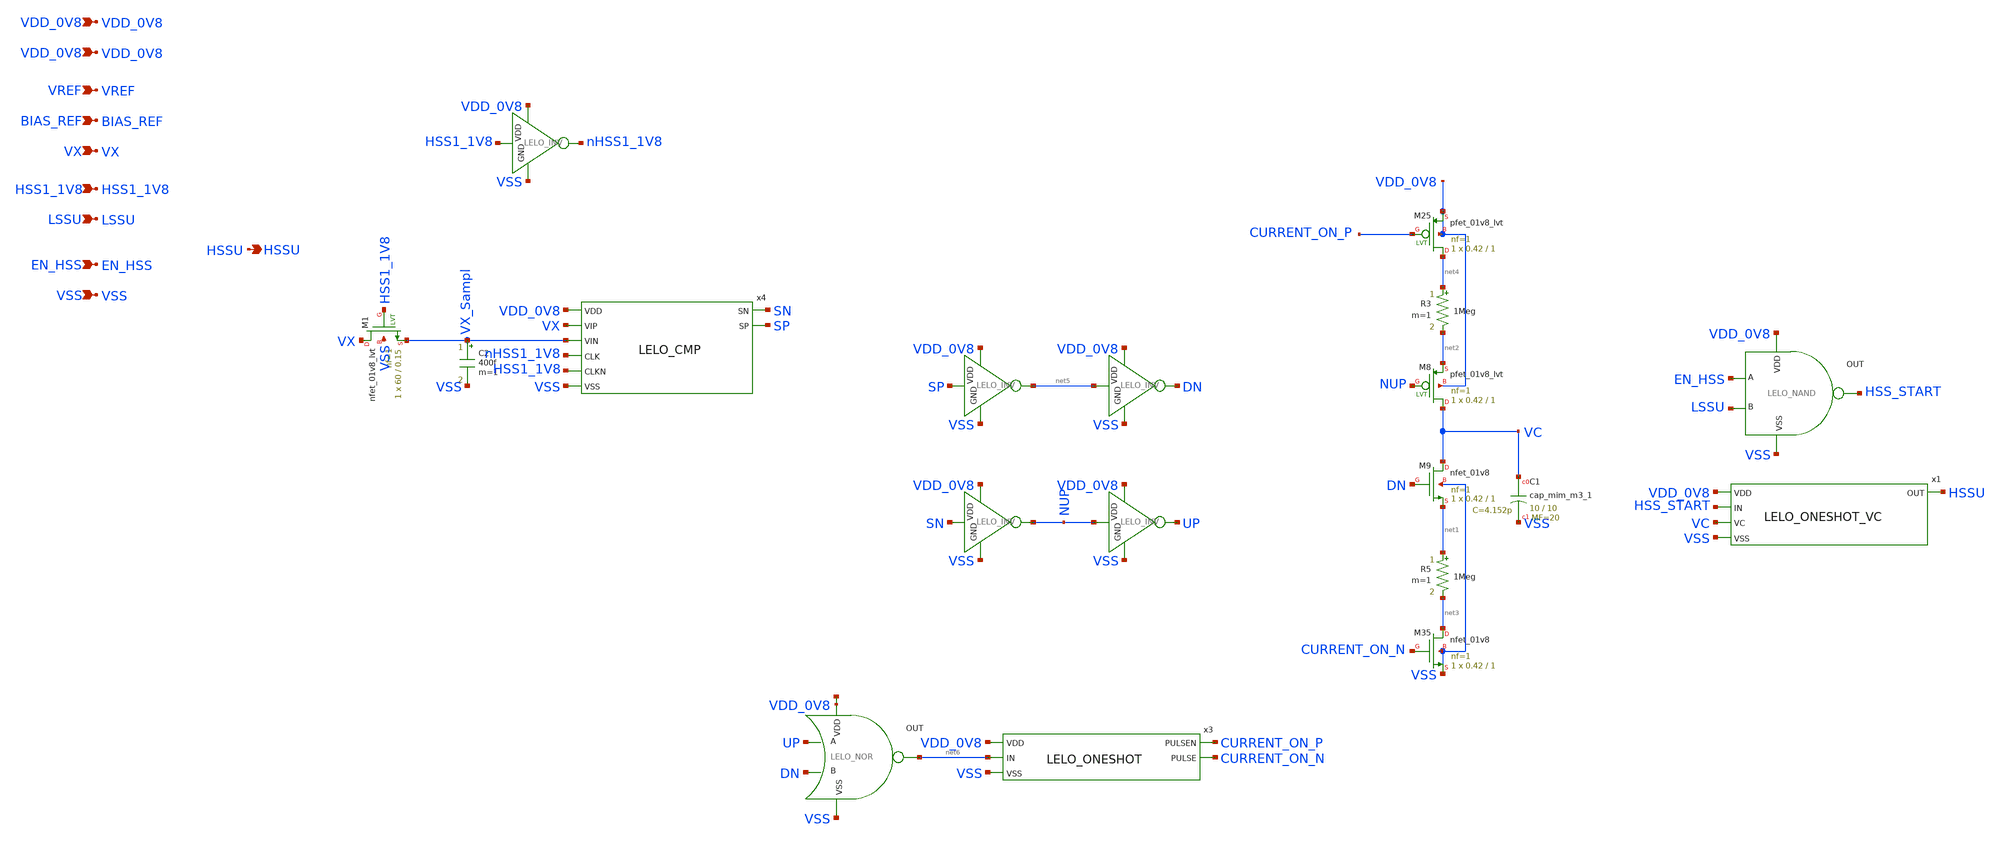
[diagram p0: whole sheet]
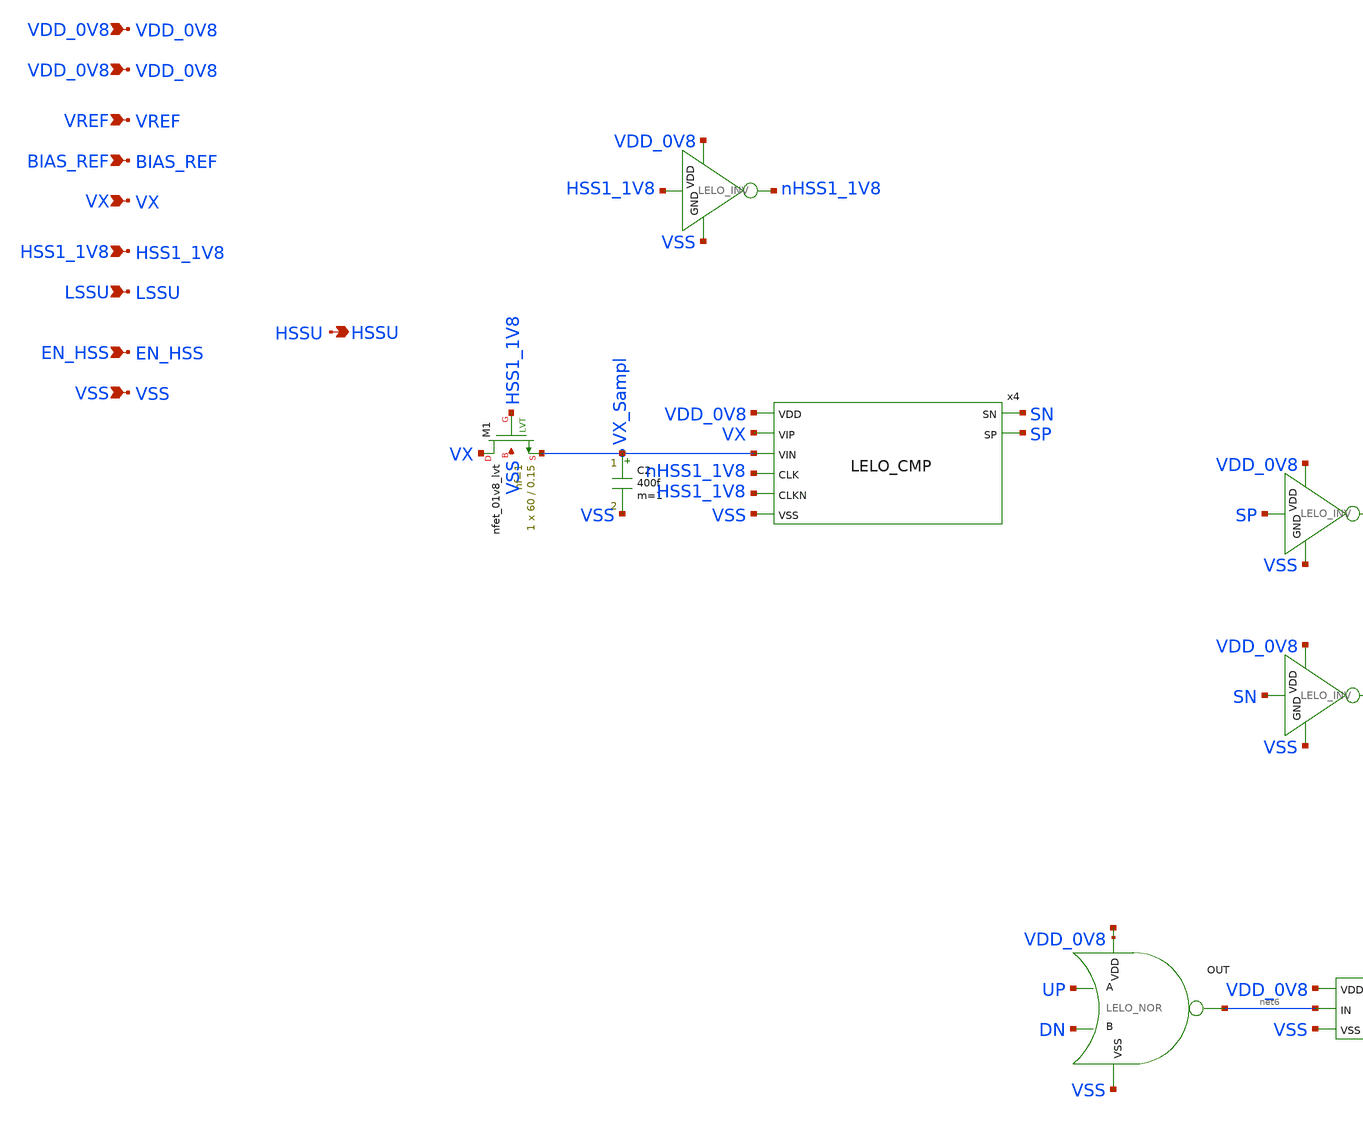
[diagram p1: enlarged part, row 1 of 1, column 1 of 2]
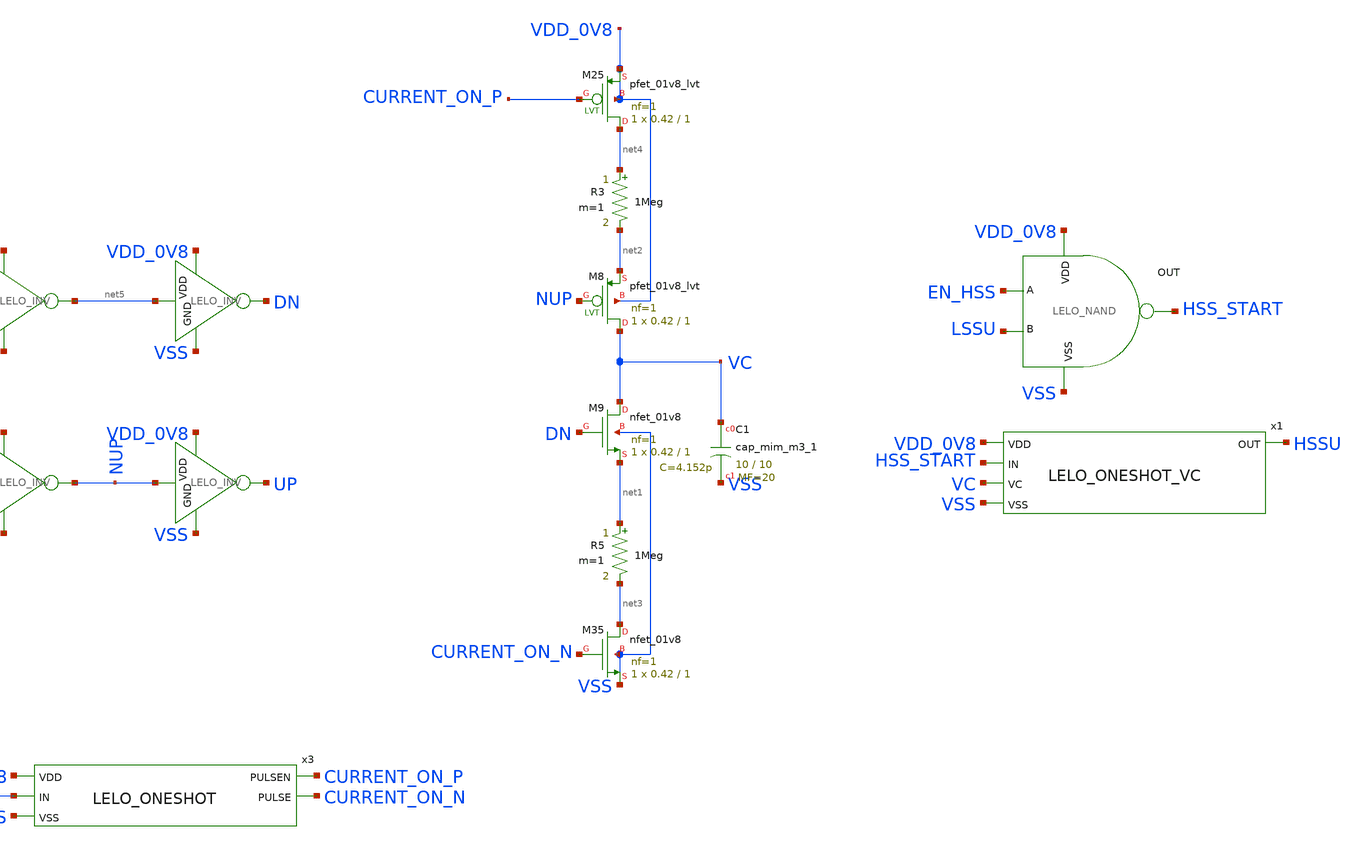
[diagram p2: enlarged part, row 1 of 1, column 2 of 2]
** sch_path: design/LELO_SVOD_SKY130A/LELO_SVOD_HSSCNTRL.sch
**.subckt LELO_SVOD_HSSCNTRL VREF HSSU VX LSSU VSS EN_HSS VDD_0V8 HSS1_1V8 BIAS_REF VDD_0V8
*.ipin VREF
*.opin HSSU
*.ipin VX
*.ipin LSSU
*.ipin VSS
*.ipin EN_HSS
*.ipin VDD_0V8
*.ipin HSS1_1V8
*.ipin BIAS_REF
*.ipin VDD_0V8
x4 SN SP VDD_0V8 VX VX_Sampl nHSS1_1V8 HSS1_1V8 VSS LELO_CMP
XM9 VC DN net1 VSS sky130_fd_pr__nfet_01v8 L=1 W=0.42 nf=1 ad='int((1 + 1)/2) * 0.42 / 1 * 0.29' as='int((1 + 2)/2) * 0.42 / 1 * 0.29'
+ pd='2*int((1 + 1)/2) * (0.42 / 1 + 0.29)' ps='2*int((1 + 2)/2) * (0.42 / 1 + 0.29)' nrd='0.29 / 0.42 '
+ nrs='0.29 / 0.42 ' sa=0 sb=0 sd=0 mult=1 m=1
x10 VDD_0V8 SP net5 VSS LELO_INV
R5 net1 net3 1Meg m=1
XM35 net3 CURRENT_ON_N VSS VSS sky130_fd_pr__nfet_01v8 L=1 W=0.42 nf=1 ad='int((1 + 1)/2) * 0.42 / 1 * 0.29'
+ as='int((1 + 2)/2) * 0.42 / 1 * 0.29' pd='2*int((1 + 1)/2) * (0.42 / 1 + 0.29)' ps='2*int((1 + 2)/2) * (0.42 / 1 + 0.29)'
+ nrd='0.29 / 0.42 ' nrs='0.29 / 0.42 ' sa=0 sb=0 sd=0 mult=1 m=1
x11 VDD_0V8 SN NUP VSS LELO_INV
x14 VDD_0V8 NUP UP VSS LELO_INV
x17 VDD_0V8 net5 DN VSS LELO_INV
x2 net7 net6 UP DN VSS LELO_NOR
x3 VDD_0V8 net6 VSS CURRENT_ON_P CURRENT_ON_N LELO_ONESHOT
R3 net4 net2 1Meg m=1
XM8 VC NUP net2 VDD_0V8 sky130_fd_pr__pfet_01v8_lvt L=1 W=0.42 nf=1 ad='int((1 + 1)/2) * 0.42 / 1 * 0.29'
+ as='int((1 + 2)/2) * 0.42 / 1 * 0.29' pd='2*int((1 + 1)/2) * (0.42 / 1 + 0.29)' ps='2*int((1 + 2)/2) * (0.42 / 1 + 0.29)'
+ nrd='0.29 / 0.42 ' nrs='0.29 / 0.42 ' sa=0 sb=0 sd=0 mult=1 m=1
XM25 net4 CURRENT_ON_P VDD_0V8 VDD_0V8 sky130_fd_pr__pfet_01v8_lvt L=1 W=0.42 nf=1 ad='int((1 + 1)/2) * 0.42 / 1 * 0.29'
+ as='int((1 + 2)/2) * 0.42 / 1 * 0.29' pd='2*int((1 + 1)/2) * (0.42 / 1 + 0.29)' ps='2*int((1 + 2)/2) * (0.42 / 1 + 0.29)'
+ nrd='0.29 / 0.42 ' nrs='0.29 / 0.42 ' sa=0 sb=0 sd=0 mult=1 m=1
x1 VDD_0V8 HSS_START VC HSSU VSS LELO_ONESHOT_VC
x6 VDD_0V8 HSS_START EN_HSS LSSU VSS LELO_NAND
XC1 VC VSS sky130_fd_pr__cap_mim_m3_1 W=10 L=10 MF=20 m=20
C2 VX_Sampl VSS 400f m=1
XM1 VX HSS1_1V8 VX_Sampl VSS sky130_fd_pr__nfet_01v8_lvt L=0.15 W=60 nf=1 ad='int((1 + 1)/2) * 60 / 1 * 0.29'
+ as='int((1 + 2)/2) * 60 / 1 * 0.29' pd='2*int((1 + 1)/2) * (60 / 1 + 0.29)' ps='2*int((1 + 2)/2) * (60 / 1 + 0.29)'
+ nrd='0.29 / 60 ' nrs='0.29 / 60 ' sa=0 sb=0 sd=0 mult=1 m=1
x5 VDD_0V8 HSS1_1V8 nHSS1_1V8 VSS LELO_INV
**.ends

* expanding   symbol:  LELO_SVOD_SKY130A/LELO_CMP.sym # of pins=8
** sym_path: design/LELO_SVOD_SKY130A/LELO_CMP.sym
** sch_path: design/LELO_SVOD_SKY130A/LELO_CMP.sch
.subckt LELO_CMP SN SP VDD VIP VIN CLK CLKN VSS
*.ipin VIP
*.ipin VIN
*.ipin CLK
*.ipin CLKN
*.ipin VDD
*.ipin VSS
*.opin SN
*.opin SP
XM2 SN net3 net5 VDD sky130_fd_pr__pfet_01v8_lvt L=0.44 W=1.92 nf=2 ad='int((2 + 1)/2) * 1.92 / 2 * 0.29'
+ as='int((2 + 2)/2) * 1.92 / 2 * 0.29' pd='2*int((2 + 1)/2) * (1.92 / 2 + 0.29)' ps='2*int((2 + 2)/2) * (1.92 / 2 + 0.29)'
+ nrd='0.29 / 1.92 ' nrs='0.29 / 1.92 ' sa=0 sb=0 sd=0 mult=3 m=3
XM1 SP net2 net6 VDD sky130_fd_pr__pfet_01v8_lvt L=0.44 W=1.92 nf=2 ad='int((2 + 1)/2) * 1.92 / 2 * 0.29'
+ as='int((2 + 2)/2) * 1.92 / 2 * 0.29' pd='2*int((2 + 1)/2) * (1.92 / 2 + 0.29)' ps='2*int((2 + 2)/2) * (1.92 / 2 + 0.29)'
+ nrd='0.29 / 1.92 ' nrs='0.29 / 1.92 ' sa=0 sb=0 sd=0 mult=3 m=3
XM3 net2 VIP net1 VSS sky130_fd_pr__nfet_01v8_lvt L=0.44 W=6.4 nf=1 ad='int((1 + 1)/2) * 6.4 / 1 * 0.29'
+ as='int((1 + 2)/2) * 6.4 / 1 * 0.29' pd='2*int((1 + 1)/2) * (6.4 / 1 + 0.29)' ps='2*int((1 + 2)/2) * (6.4 / 1 + 0.29)'
+ nrd='0.29 / 6.4 ' nrs='0.29 / 6.4 ' sa=0 sb=0 sd=0 mult=1 m=1
XM4 net3 VIN net1 VSS sky130_fd_pr__nfet_01v8_lvt L=0.44 W=6.4 nf=1 ad='int((1 + 1)/2) * 6.4 / 1 * 0.29'
+ as='int((1 + 2)/2) * 6.4 / 1 * 0.29' pd='2*int((1 + 1)/2) * (6.4 / 1 + 0.29)' ps='2*int((1 + 2)/2) * (6.4 / 1 + 0.29)'
+ nrd='0.29 / 6.4 ' nrs='0.29 / 6.4 ' sa=0 sb=0 sd=0 mult=1 m=1
XM5 net3 CLK VDD VDD sky130_fd_pr__pfet_01v8_lvt L=0.94 W=1.92 nf=2 ad='int((2 + 1)/2) * 1.92 / 2 * 0.29'
+ as='int((2 + 2)/2) * 1.92 / 2 * 0.29' pd='2*int((2 + 1)/2) * (1.92 / 2 + 0.29)' ps='2*int((2 + 2)/2) * (1.92 / 2 + 0.29)'
+ nrd='0.29 / 1.92 ' nrs='0.29 / 1.92 ' sa=0 sb=0 sd=0 mult=1 m=1
XM6 net6 SN VDD VDD sky130_fd_pr__pfet_01v8_lvt L=0.94 W=1.92 nf=2 ad='int((2 + 1)/2) * 1.92 / 2 * 0.29'
+ as='int((2 + 2)/2) * 1.92 / 2 * 0.29' pd='2*int((2 + 1)/2) * (1.92 / 2 + 0.29)' ps='2*int((2 + 2)/2) * (1.92 / 2 + 0.29)'
+ nrd='0.29 / 1.92 ' nrs='0.29 / 1.92 ' sa=0 sb=0 sd=0 mult=1 m=1
XM7 net5 SP VDD VDD sky130_fd_pr__pfet_01v8_lvt L=0.94 W=1.92 nf=2 ad='int((2 + 1)/2) * 1.92 / 2 * 0.29'
+ as='int((2 + 2)/2) * 1.92 / 2 * 0.29' pd='2*int((2 + 1)/2) * (1.92 / 2 + 0.29)' ps='2*int((2 + 2)/2) * (1.92 / 2 + 0.29)'
+ nrd='0.29 / 1.92 ' nrs='0.29 / 1.92 ' sa=0 sb=0 sd=0 mult=1 m=1
XM8 net2 CLK VDD VDD sky130_fd_pr__pfet_01v8_lvt L=0.94 W=1.92 nf=2 ad='int((2 + 1)/2) * 1.92 / 2 * 0.29'
+ as='int((2 + 2)/2) * 1.92 / 2 * 0.29' pd='2*int((2 + 1)/2) * (1.92 / 2 + 0.29)' ps='2*int((2 + 2)/2) * (1.92 / 2 + 0.29)'
+ nrd='0.29 / 1.92 ' nrs='0.29 / 1.92 ' sa=0 sb=0 sd=0 mult=1 m=1
XM9 net1 CLK net4 VSS sky130_fd_pr__nfet_01v8 L=0.94 W=1.92 nf=2 ad='int((2 + 1)/2) * 1.92 / 2 * 0.29'
+ as='int((2 + 2)/2) * 1.92 / 2 * 0.29' pd='2*int((2 + 1)/2) * (1.92 / 2 + 0.29)' ps='2*int((2 + 2)/2) * (1.92 / 2 + 0.29)'
+ nrd='0.29 / 1.92 ' nrs='0.29 / 1.92 ' sa=0 sb=0 sd=0 mult=1 m=1
XM10 net4 CLK VSS VSS sky130_fd_pr__nfet_01v8 L=0.94 W=1.92 nf=2 ad='int((2 + 1)/2) * 1.92 / 2 * 0.29'
+ as='int((2 + 2)/2) * 1.92 / 2 * 0.29' pd='2*int((2 + 1)/2) * (1.92 / 2 + 0.29)' ps='2*int((2 + 2)/2) * (1.92 / 2 + 0.29)'
+ nrd='0.29 / 1.92 ' nrs='0.29 / 1.92 ' sa=0 sb=0 sd=0 mult=1 m=1
XM11 SN CLKN VSS VSS sky130_fd_pr__nfet_01v8 L=0.94 W=1.92 nf=2 ad='int((2 + 1)/2) * 1.92 / 2 * 0.29'
+ as='int((2 + 2)/2) * 1.92 / 2 * 0.29' pd='2*int((2 + 1)/2) * (1.92 / 2 + 0.29)' ps='2*int((2 + 2)/2) * (1.92 / 2 + 0.29)'
+ nrd='0.29 / 1.92 ' nrs='0.29 / 1.92 ' sa=0 sb=0 sd=0 mult=1 m=1
XM12 SP SN VSS VSS sky130_fd_pr__nfet_01v8 L=0.94 W=1.92 nf=2 ad='int((2 + 1)/2) * 1.92 / 2 * 0.29' as='int((2 + 2)/2) * 1.92 / 2 * 0.29'
+ pd='2*int((2 + 1)/2) * (1.92 / 2 + 0.29)' ps='2*int((2 + 2)/2) * (1.92 / 2 + 0.29)' nrd='0.29 / 1.92 '
+ nrs='0.29 / 1.92 ' sa=0 sb=0 sd=0 mult=1 m=1
XM13 SN SP VSS VSS sky130_fd_pr__nfet_01v8 L=0.94 W=1.92 nf=2 ad='int((2 + 1)/2) * 1.92 / 2 * 0.29' as='int((2 + 2)/2) * 1.92 / 2 * 0.29'
+ pd='2*int((2 + 1)/2) * (1.92 / 2 + 0.29)' ps='2*int((2 + 2)/2) * (1.92 / 2 + 0.29)' nrd='0.29 / 1.92 '
+ nrs='0.29 / 1.92 ' sa=0 sb=0 sd=0 mult=1 m=1
XM14 SP CLKN VSS VSS sky130_fd_pr__nfet_01v8 L=0.94 W=1.92 nf=2 ad='int((2 + 1)/2) * 1.92 / 2 * 0.29'
+ as='int((2 + 2)/2) * 1.92 / 2 * 0.29' pd='2*int((2 + 1)/2) * (1.92 / 2 + 0.29)' ps='2*int((2 + 2)/2) * (1.92 / 2 + 0.29)'
+ nrd='0.29 / 1.92 ' nrs='0.29 / 1.92 ' sa=0 sb=0 sd=0 mult=1 m=1
.ends


* expanding   symbol:  LELO_SVOD_SKY130A/LELO_INV.sym # of pins=4
** sym_path: design/LELO_SVOD_SKY130A/LELO_INV.sym
** sch_path: design/LELO_SVOD_SKY130A/LELO_INV.sch
.subckt LELO_INV VDD VIN VOUT GND
*.ipin VIN
*.ipin VDD
*.ipin GND
*.opin VOUT
XM1 VOUT VIN GND GND sky130_fd_pr__nfet_01v8_lvt L=0.15 W=1 nf=1 ad='int((1 + 1)/2) * 1 / 1 * 0.29' as='int((1 + 2)/2) * 1 / 1 * 0.29'
+ pd='2*int((1 + 1)/2) * (1 / 1 + 0.29)' ps='2*int((1 + 2)/2) * (1 / 1 + 0.29)' nrd='0.29 / 1 ' nrs='0.29 / 1 '
+ sa=0 sb=0 sd=0 mult=1 m=1
XM2 VOUT VIN VDD VDD sky130_fd_pr__pfet_01v8_lvt L=0.35 W=1 nf=1 ad='int((1 + 1)/2) * 1 / 1 * 0.29' as='int((1 + 2)/2) * 1 / 1 * 0.29'
+ pd='2*int((1 + 1)/2) * (1 / 1 + 0.29)' ps='2*int((1 + 2)/2) * (1 / 1 + 0.29)' nrd='0.29 / 1 ' nrs='0.29 / 1 '
+ sa=0 sb=0 sd=0 mult=2 m=2
.ends


* expanding   symbol:  LELO_SVOD_SKY130A/LELO_NOR.sym # of pins=5
** sym_path: design/LELO_SVOD_SKY130A/LELO_NOR.sym
** sch_path: design/LELO_SVOD_SKY130A/LELO_NOR.sch
.subckt LELO_NOR VDD OUT A B VSS
*.ipin VDD
*.ipin VSS
*.opin OUT
*.ipin A
*.ipin B
XM2 OUT B VSS VSS sky130_fd_pr__nfet_01v8 L=0.15 W=2 nf=1 ad='int((1 + 1)/2) * 2 / 1 * 0.29' as='int((1 + 2)/2) * 2 / 1 * 0.29'
+ pd='2*int((1 + 1)/2) * (2 / 1 + 0.29)' ps='2*int((1 + 2)/2) * (2 / 1 + 0.29)' nrd='0.29 / 2 ' nrs='0.29 / 2 '
+ sa=0 sb=0 sd=0 mult=1 m=1
XM1 OUT A VSS VSS sky130_fd_pr__nfet_01v8 L=0.15 W=2 nf=1 ad='int((1 + 1)/2) * 2 / 1 * 0.29' as='int((1 + 2)/2) * 2 / 1 * 0.29'
+ pd='2*int((1 + 1)/2) * (2 / 1 + 0.29)' ps='2*int((1 + 2)/2) * (2 / 1 + 0.29)' nrd='0.29 / 2 ' nrs='0.29 / 2 '
+ sa=0 sb=0 sd=0 mult=1 m=1
XM3 OUT B net1 VDD sky130_fd_pr__pfet_01v8 L=0.15 W=4 nf=1 ad='int((1 + 1)/2) * 4 / 1 * 0.29' as='int((1 + 2)/2) * 4 / 1 * 0.29'
+ pd='2*int((1 + 1)/2) * (4 / 1 + 0.29)' ps='2*int((1 + 2)/2) * (4 / 1 + 0.29)' nrd='0.29 / 4 ' nrs='0.29 / 4 '
+ sa=0 sb=0 sd=0 mult=1 m=1
XM4 net1 A VDD VDD sky130_fd_pr__pfet_01v8 L=0.15 W=4 nf=1 ad='int((1 + 1)/2) * 4 / 1 * 0.29' as='int((1 + 2)/2) * 4 / 1 * 0.29'
+ pd='2*int((1 + 1)/2) * (4 / 1 + 0.29)' ps='2*int((1 + 2)/2) * (4 / 1 + 0.29)' nrd='0.29 / 4 ' nrs='0.29 / 4 '
+ sa=0 sb=0 sd=0 mult=1 m=1
.ends


* expanding   symbol:  LELO_SVOD_SKY130A/LELO_ONESHOT.sym # of pins=5
** sym_path: design/LELO_SVOD_SKY130A/LELO_ONESHOT.sym
** sch_path: design/LELO_SVOD_SKY130A/LELO_ONESHOT.sch
.subckt LELO_ONESHOT VDD IN VSS PULSEN PULSE
*.ipin VDD
*.ipin IN
*.ipin VSS
*.opin PULSEN
*.opin PULSE
x8 VDD PULSEN PULSE VSS LELO_INV
x12 net6 net3 net1 PULSE VSS LELO_NOR
C6 net2 net4 150f m=1
x13 VDD net2 PULSEN VSS LELO_INV
x18 VDD IN net1 VSS LELO_INV
x1 VDD net3 net4 VSS LELO_INV
XM1 net2 VDD net5 net5 sky130_fd_pr__nfet_01v8 L=0.15 W=1 nf=1 ad='int((1 + 1)/2) * 1 / 1 * 0.29' as='int((1 + 2)/2) * 1 / 1 * 0.29'
+ pd='2*int((1 + 1)/2) * (1 / 1 + 0.29)' ps='2*int((1 + 2)/2) * (1 / 1 + 0.29)' nrd='0.29 / 1 ' nrs='0.29 / 1 '
+ sa=0 sb=0 sd=0 mult=1 m=1
x2 VDD net3 net4 VSS LELO_INV
XR1 VSS net5 net5 sky130_fd_pr__res_xhigh_po_0p35 L=30 mult=1 m=1
.ends


* expanding   symbol:  LELO_SVOD_SKY130A/LELO_ONESHOT_VC.sym # of pins=5
** sym_path: design/LELO_SVOD_SKY130A/LELO_ONESHOT_VC.sym
** sch_path: design/LELO_SVOD_SKY130A/LELO_ONESHOT_VC.sch
.subckt LELO_ONESHOT_VC VDD IN VC OUT VSS
*.ipin VDD
*.ipin IN
*.ipin VC
*.ipin VSS
*.opin OUT
x2 net6 net2 OUT IN VSS LELO_NOR
C5 net1 net3 300f m=1
XM1 net1 VDD net5 net5 sky130_fd_pr__nfet_01v8 L=0.15 W=1 nf=1 ad='int((1 + 1)/2) * 1 / 1 * 0.29' as='int((1 + 2)/2) * 1 / 1 * 0.29'
+ pd='2*int((1 + 1)/2) * (1 / 1 + 0.29)' ps='2*int((1 + 2)/2) * (1 / 1 + 0.29)' nrd='0.29 / 1 ' nrs='0.29 / 1 '
+ sa=0 sb=0 sd=0 mult=1 m=1
XM2 net1 VC VSS VSS sky130_fd_pr__nfet_05v0_nvt L=20 W=0.5 nf=1 ad='int((1 + 1)/2) * 0.5 / 1 * 0.29'
+ as='int((1 + 2)/2) * 0.5 / 1 * 0.29' pd='2*int((1 + 1)/2) * (0.5 / 1 + 0.29)' ps='2*int((1 + 2)/2) * (0.5 / 1 + 0.29)'
+ nrd='0.29 / 0.5 ' nrs='0.29 / 0.5 ' sa=0 sb=0 sd=0 mult=1 m=1
XR1 VSS net5 net5 sky130_fd_pr__res_xhigh_po_0p35 L=150 mult=1 m=1
x1 VDD net1 net4 VSS LELO_INV_PVT
x3 VDD net4 OUT VSS LELO_INV_PVT
x4 VDD net2 net3 VSS LELO_INV
.ends


* expanding   symbol:  LELO_SVOD_SKY130A/LELO_NAND.sym # of pins=5
** sym_path: design/LELO_SVOD_SKY130A/LELO_NAND.sym
** sch_path: design/LELO_SVOD_SKY130A/LELO_NAND.sch
.subckt LELO_NAND VDD OUT A B VSS
*.ipin VDD
*.ipin VSS
*.opin OUT
*.ipin A
*.ipin B
XM1 net1 A VSS VSS sky130_fd_pr__nfet_01v8_lvt L=0.15 W=1 nf=1 ad='int((1 + 1)/2) * 1 / 1 * 0.29' as='int((1 + 2)/2) * 1 / 1 * 0.29'
+ pd='2*int((1 + 1)/2) * (1 / 1 + 0.29)' ps='2*int((1 + 2)/2) * (1 / 1 + 0.29)' nrd='0.29 / 1 ' nrs='0.29 / 1 '
+ sa=0 sb=0 sd=0 mult=1 m=1
XM2 OUT B net1 net1 sky130_fd_pr__nfet_01v8_lvt L=0.15 W=1 nf=1 ad='int((1 + 1)/2) * 1 / 1 * 0.29' as='int((1 + 2)/2) * 1 / 1 * 0.29'
+ pd='2*int((1 + 1)/2) * (1 / 1 + 0.29)' ps='2*int((1 + 2)/2) * (1 / 1 + 0.29)' nrd='0.29 / 1 ' nrs='0.29 / 1 '
+ sa=0 sb=0 sd=0 mult=1 m=1
XM3 OUT A VDD VDD sky130_fd_pr__pfet_01v8_lvt L=0.35 W=1 nf=1 ad='int((1 + 1)/2) * 1 / 1 * 0.29' as='int((1 + 2)/2) * 1 / 1 * 0.29'
+ pd='2*int((1 + 1)/2) * (1 / 1 + 0.29)' ps='2*int((1 + 2)/2) * (1 / 1 + 0.29)' nrd='0.29 / 1 ' nrs='0.29 / 1 '
+ sa=0 sb=0 sd=0 mult=1 m=1
XM4 OUT B VDD VDD sky130_fd_pr__pfet_01v8_lvt L=0.35 W=1 nf=1 ad='int((1 + 1)/2) * 1 / 1 * 0.29' as='int((1 + 2)/2) * 1 / 1 * 0.29'
+ pd='2*int((1 + 1)/2) * (1 / 1 + 0.29)' ps='2*int((1 + 2)/2) * (1 / 1 + 0.29)' nrd='0.29 / 1 ' nrs='0.29 / 1 '
+ sa=0 sb=0 sd=0 mult=1 m=1
.ends


* expanding   symbol:  LELO_SVOD_SKY130A/LELO_INV_PVT.sym # of pins=4
** sym_path: design/LELO_SVOD_SKY130A/LELO_INV_PVT.sym
** sch_path: design/LELO_SVOD_SKY130A/LELO_INV_PVT.sch
.subckt LELO_INV_PVT VDD VIN VOUT VSS
*.ipin VIN
*.ipin VDD
*.ipin VSS
*.opin VOUT
XM1 VOUT VIN VSS VSS sky130_fd_pr__nfet_01v8 L=0.5 W=4 nf=1 ad='int((1 + 1)/2) * 4 / 1 * 0.29' as='int((1 + 2)/2) * 4 / 1 * 0.29'
+ pd='2*int((1 + 1)/2) * (4 / 1 + 0.29)' ps='2*int((1 + 2)/2) * (4 / 1 + 0.29)' nrd='0.29 / 4 ' nrs='0.29 / 4 '
+ sa=0 sb=0 sd=0 mult=1 m=1
XM2 VOUT VIN VDD VDD sky130_fd_pr__pfet_01v8_lvt L=1 W=4 nf=1 ad='int((1 + 1)/2) * 4 / 1 * 0.29' as='int((1 + 2)/2) * 4 / 1 * 0.29'
+ pd='2*int((1 + 1)/2) * (4 / 1 + 0.29)' ps='2*int((1 + 2)/2) * (4 / 1 + 0.29)' nrd='0.29 / 4 ' nrs='0.29 / 4 '
+ sa=0 sb=0 sd=0 mult=1 m=1
.ends

.end
